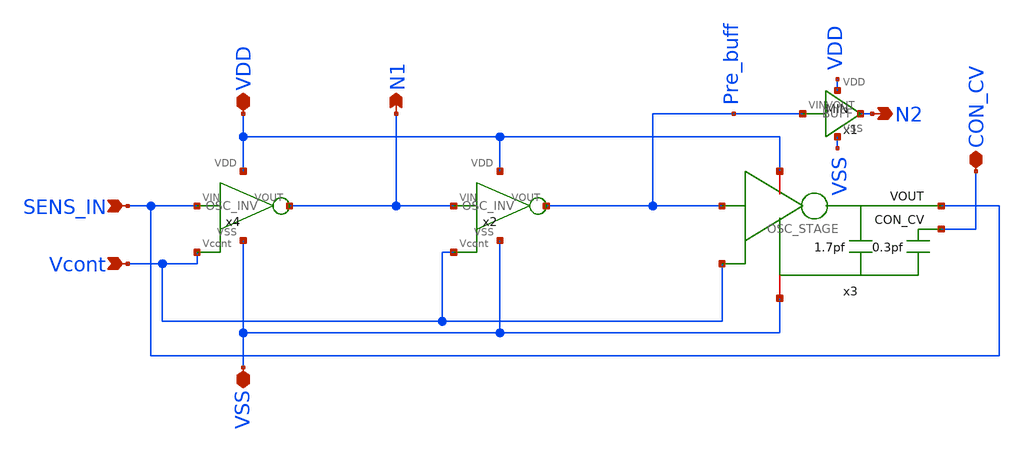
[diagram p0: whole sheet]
** sch_path: ABC123_SDC/design_data/xschem/OSC_STAGE/OSC_RING.sch
**.subckt OSC_RING SENS_IN VDD VSS N1 N2 CON_CV Vcont
*.ipin SENS_IN
*.iopin VDD
*.iopin VSS
*.opin N1
*.opin N2
*.iopin CON_CV
*.ipin Vcont
x3 VDD CON_CV SENS_IN Pre_buff VSS Vcont OSC_STAGE
x1 Pre_buff N2 VDD VSS BUFF
x4 VDD SENS_IN N1 VSS Vcont OSC_INV
x2 VDD N1 Pre_buff VSS Vcont OSC_INV
**.ends
.end
